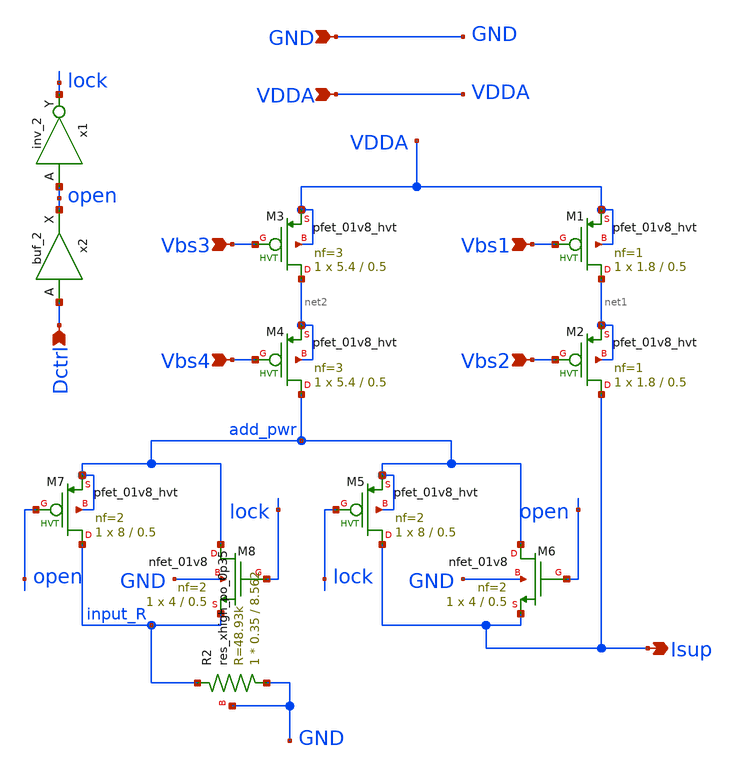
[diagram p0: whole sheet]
** sch_path: xschem/lib/ALib_IDAC.sch
**.subckt ALib_IDAC Vbs3 Vbs4 Vbs1 Vbs2 Isup Dctrl GND VDDA
*.ipin Vbs3
*.ipin Vbs4
*.ipin Vbs1
*.ipin Vbs2
*.opin Isup
*.ipin Dctrl
*.ipin GND
*.ipin VDDA
x1 open GND GND VDDA VDDA lock sky130_fd_sc_hd__inv_2
XM1 net1 Vbs1 VDDA VDDA sky130_fd_pr__pfet_01v8_hvt L=0.5 W=1.8 nf=1 ad='int((1 + 1)/2) * 1.8 / 1 * 0.29'
+ as='int((1 + 2)/2) * 1.8 / 1 * 0.29' pd='2*int((1 + 1)/2) * (1.8 / 1 + 0.29)' ps='2*int((1 + 2)/2) * (1.8 / 1 + 0.29)'
+ nrd='0.29 / 1.8 ' nrs='0.29 / 1.8 ' sa=0 sb=0 sd=0 mult=1 m=1
XM2 Isup Vbs2 net1 net1 sky130_fd_pr__pfet_01v8_hvt L=0.5 W=1.8 nf=1 ad='int((1 + 1)/2) * 1.8 / 1 * 0.29'
+ as='int((1 + 2)/2) * 1.8 / 1 * 0.29' pd='2*int((1 + 1)/2) * (1.8 / 1 + 0.29)' ps='2*int((1 + 2)/2) * (1.8 / 1 + 0.29)'
+ nrd='0.29 / 1.8 ' nrs='0.29 / 1.8 ' sa=0 sb=0 sd=0 mult=1 m=1
x2 Dctrl GND GND VDDA VDDA open sky130_fd_sc_hd__buf_2
XM3 net2 Vbs3 VDDA VDDA sky130_fd_pr__pfet_01v8_hvt L=0.5 W=5.4 nf=3 ad='int((3 + 1)/2) * 5.4 / 3 * 0.29'
+ as='int((3 + 2)/2) * 5.4 / 3 * 0.29' pd='2*int((3 + 1)/2) * (5.4 / 3 + 0.29)' ps='2*int((3 + 2)/2) * (5.4 / 3 + 0.29)'
+ nrd='0.29 / 5.4 ' nrs='0.29 / 5.4 ' sa=0 sb=0 sd=0 mult=1 m=1
XM4 add_pwr Vbs4 net2 net2 sky130_fd_pr__pfet_01v8_hvt L=0.5 W=5.4 nf=3 ad='int((3 + 1)/2) * 5.4 / 3 * 0.29'
+ as='int((3 + 2)/2) * 5.4 / 3 * 0.29' pd='2*int((3 + 1)/2) * (5.4 / 3 + 0.29)' ps='2*int((3 + 2)/2) * (5.4 / 3 + 0.29)'
+ nrd='0.29 / 5.4 ' nrs='0.29 / 5.4 ' sa=0 sb=0 sd=0 mult=1 m=1
XM5 Isup lock add_pwr add_pwr sky130_fd_pr__pfet_01v8_hvt L=0.5 W=8 nf=2 ad='int((2 + 1)/2) * 8 / 2 * 0.29'
+ as='int((2 + 2)/2) * 8 / 2 * 0.29' pd='2*int((2 + 1)/2) * (8 / 2 + 0.29)' ps='2*int((2 + 2)/2) * (8 / 2 + 0.29)'
+ nrd='0.29 / 8 ' nrs='0.29 / 8 ' sa=0 sb=0 sd=0 mult=1 m=1
XM6 add_pwr open Isup GND sky130_fd_pr__nfet_01v8 L=0.5 W=4 nf=2 ad='int((nf+1)/2) * W/nf * 0.29' as='int((nf+2)/2) * W/nf * 0.29'
+ pd='2*int((nf+1)/2) * (W/nf + 0.29)' ps='2*int((nf+2)/2) * (W/nf + 0.29)' nrd='0.29 / W' nrs='0.29 / W'
+ sa=0 sb=0 sd=0 mult=1 m=1
XM7 input_R open add_pwr add_pwr sky130_fd_pr__pfet_01v8_hvt L=0.5 W=8 nf=2 ad='int((2 + 1)/2) * 8 / 2 * 0.29'
+ as='int((2 + 2)/2) * 8 / 2 * 0.29' pd='2*int((2 + 1)/2) * (8 / 2 + 0.29)' ps='2*int((2 + 2)/2) * (8 / 2 + 0.29)'
+ nrd='0.29 / 8 ' nrs='0.29 / 8 ' sa=0 sb=0 sd=0 mult=1 m=1
XM8 add_pwr lock input_R GND sky130_fd_pr__nfet_01v8 L=0.5 W=4 nf=2 ad='int((nf+1)/2) * W/nf * 0.29'
+ as='int((nf+2)/2) * W/nf * 0.29' pd='2*int((nf+1)/2) * (W/nf + 0.29)' ps='2*int((nf+2)/2) * (W/nf + 0.29)'
+ nrd='0.29 / W' nrs='0.29 / W' sa=0 sb=0 sd=0 mult=1 m=1
XR2 GND input_R GND sky130_fd_pr__res_xhigh_po_0p35 L=8.562 mult=1 m=1
**.ends
.end
